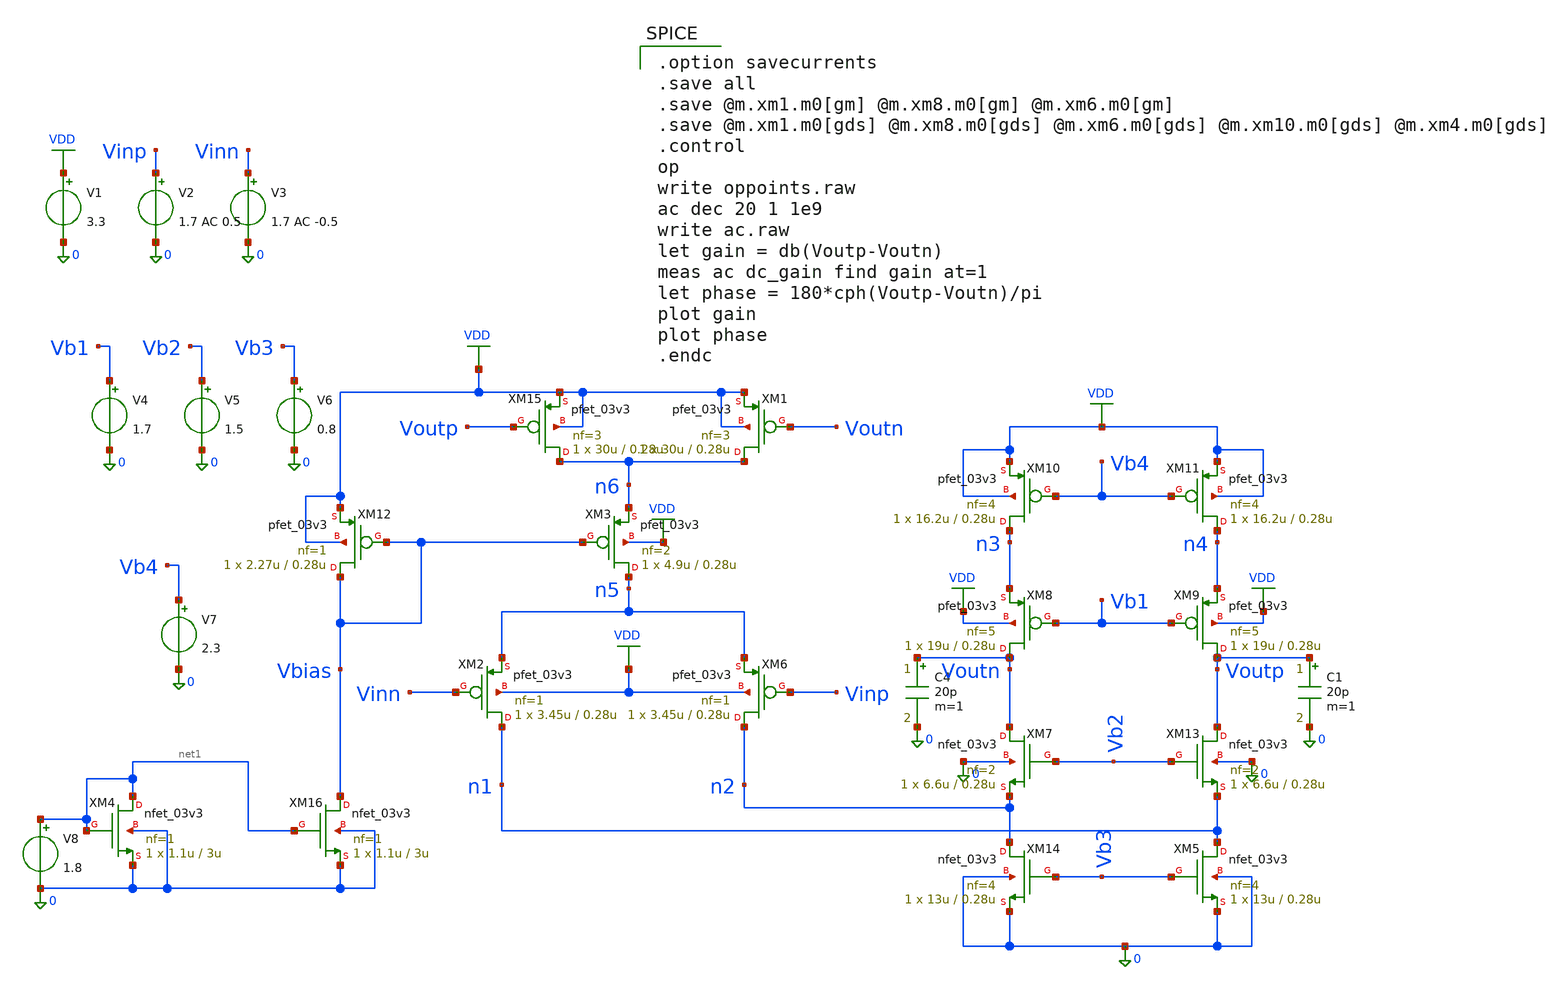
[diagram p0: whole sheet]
** sch_path: jz_fda2/xschem/foldedcasc_cmfb_forlayout_CMcheck.sch
**.subckt foldedcasc_cmfb_forlayout_CMcheck
V1 VDD 0 3.3
V2 Vinp 0 1.7 AC 0.5
C4 Voutn 0 20p m=1
C1 Voutp 0 20p m=1
V3 Vinn 0 1.7 AC -0.5
V4 Vb1 0 1.7
V5 Vb2 0 1.5
V6 Vb3 0 0.8
V7 Vb4 0 2.3
XM15 n6 Voutp VDD VDD pfet_03v3 L=0.28u W=30u nf=3 ad='int((nf+1)/2) * W/nf * 0.18u' as='int((nf+2)/2) * W/nf * 0.18u'
+ pd='2*int((nf+1)/2) * (W/nf + 0.18u)' ps='2*int((nf+2)/2) * (W/nf + 0.18u)' nrd='0.18u / W' nrs='0.18u / W'
+ sa=0 sb=0 sd=0 m=1
XM1 n6 Voutn VDD VDD pfet_03v3 L=0.28u W=30u nf=3 ad='int((nf+1)/2) * W/nf * 0.18u' as='int((nf+2)/2) * W/nf * 0.18u'
+ pd='2*int((nf+1)/2) * (W/nf + 0.18u)' ps='2*int((nf+2)/2) * (W/nf + 0.18u)' nrd='0.18u / W' nrs='0.18u / W'
+ sa=0 sb=0 sd=0 m=1
XM12 Vbias Vbias VDD VDD pfet_03v3 L=0.28u W=2.27u nf=1 ad='int((nf+1)/2) * W/nf * 0.18u' as='int((nf+2)/2) * W/nf * 0.18u'
+ pd='2*int((nf+1)/2) * (W/nf + 0.18u)' ps='2*int((nf+2)/2) * (W/nf + 0.18u)' nrd='0.18u / W' nrs='0.18u / W'
+ sa=0 sb=0 sd=0 m=1
XM3 n5 Vbias n6 VDD pfet_03v3 L=0.28u W=4.9u nf=2 ad='int((nf+1)/2) * W/nf * 0.18u' as='int((nf+2)/2) * W/nf * 0.18u'
+ pd='2*int((nf+1)/2) * (W/nf + 0.18u)' ps='2*int((nf+2)/2) * (W/nf + 0.18u)' nrd='0.18u / W' nrs='0.18u / W'
+ sa=0 sb=0 sd=0 m=1
XM2 n1 Vinn n5 VDD pfet_03v3 L=0.28u W=3.45u nf=1 ad='int((nf+1)/2) * W/nf * 0.18u' as='int((nf+2)/2) * W/nf * 0.18u'
+ pd='2*int((nf+1)/2) * (W/nf + 0.18u)' ps='2*int((nf+2)/2) * (W/nf + 0.18u)' nrd='0.18u / W' nrs='0.18u / W'
+ sa=0 sb=0 sd=0 m=1
XM6 n2 Vinp n5 VDD pfet_03v3 L=0.28u W=3.45u nf=1 ad='int((nf+1)/2) * W/nf * 0.18u' as='int((nf+2)/2) * W/nf * 0.18u'
+ pd='2*int((nf+1)/2) * (W/nf + 0.18u)' ps='2*int((nf+2)/2) * (W/nf + 0.18u)' nrd='0.18u / W' nrs='0.18u / W'
+ sa=0 sb=0 sd=0 m=1
XM10 n3 Vb4 VDD VDD pfet_03v3 L=0.28u W=16.2u nf=4 ad='int((nf+1)/2) * W/nf * 0.18u' as='int((nf+2)/2) * W/nf * 0.18u'
+ pd='2*int((nf+1)/2) * (W/nf + 0.18u)' ps='2*int((nf+2)/2) * (W/nf + 0.18u)' nrd='0.18u / W' nrs='0.18u / W'
+ sa=0 sb=0 sd=0 m=1
XM11 n4 Vb4 VDD VDD pfet_03v3 L=0.28u W=16.2u nf=4 ad='int((nf+1)/2) * W/nf * 0.18u' as='int((nf+2)/2) * W/nf * 0.18u'
+ pd='2*int((nf+1)/2) * (W/nf + 0.18u)' ps='2*int((nf+2)/2) * (W/nf + 0.18u)' nrd='0.18u / W' nrs='0.18u / W'
+ sa=0 sb=0 sd=0 m=1
XM8 Voutn Vb1 n3 VDD pfet_03v3 L=0.28u W=19u nf=5 ad='int((nf+1)/2) * W/nf * 0.18u' as='int((nf+2)/2) * W/nf * 0.18u'
+ pd='2*int((nf+1)/2) * (W/nf + 0.18u)' ps='2*int((nf+2)/2) * (W/nf + 0.18u)' nrd='0.18u / W' nrs='0.18u / W'
+ sa=0 sb=0 sd=0 m=1
XM9 Voutp Vb1 n4 VDD pfet_03v3 L=0.28u W=19u nf=5 ad='int((nf+1)/2) * W/nf * 0.18u' as='int((nf+2)/2) * W/nf * 0.18u'
+ pd='2*int((nf+1)/2) * (W/nf + 0.18u)' ps='2*int((nf+2)/2) * (W/nf + 0.18u)' nrd='0.18u / W' nrs='0.18u / W'
+ sa=0 sb=0 sd=0 m=1
XM7 Voutn Vb2 n2 0 nfet_03v3 L=0.28u W=6.6u nf=2 ad='int((nf+1)/2) * W/nf * 0.18u' as='int((nf+2)/2) * W/nf * 0.18u'
+ pd='2*int((nf+1)/2) * (W/nf + 0.18u)' ps='2*int((nf+2)/2) * (W/nf + 0.18u)' nrd='0.18u / W' nrs='0.18u / W'
+ sa=0 sb=0 sd=0 m=1
XM13 Voutp Vb2 n1 0 nfet_03v3 L=0.28u W=6.6u nf=2 ad='int((nf+1)/2) * W/nf * 0.18u' as='int((nf+2)/2) * W/nf * 0.18u'
+ pd='2*int((nf+1)/2) * (W/nf + 0.18u)' ps='2*int((nf+2)/2) * (W/nf + 0.18u)' nrd='0.18u / W' nrs='0.18u / W'
+ sa=0 sb=0 sd=0 m=1
XM14 n2 Vb3 0 0 nfet_03v3 L=0.28u W=13u nf=4 ad='int((nf+1)/2) * W/nf * 0.18u' as='int((nf+2)/2) * W/nf * 0.18u'
+ pd='2*int((nf+1)/2) * (W/nf + 0.18u)' ps='2*int((nf+2)/2) * (W/nf + 0.18u)' nrd='0.18u / W' nrs='0.18u / W'
+ sa=0 sb=0 sd=0 m=1
XM5 n1 Vb3 0 0 nfet_03v3 L=0.28u W=13u nf=4 ad='int((nf+1)/2) * W/nf * 0.18u' as='int((nf+2)/2) * W/nf * 0.18u'
+ pd='2*int((nf+1)/2) * (W/nf + 0.18u)' ps='2*int((nf+2)/2) * (W/nf + 0.18u)' nrd='0.18u / W' nrs='0.18u / W'
+ sa=0 sb=0 sd=0 m=1
V8 net1 0 1.8
XM4 net1 net1 0 0 nfet_03v3 L=3u W=1.1u nf=1 ad='int((nf+1)/2) * W/nf * 0.18u' as='int((nf+2)/2) * W/nf * 0.18u'
+ pd='2*int((nf+1)/2) * (W/nf + 0.18u)' ps='2*int((nf+2)/2) * (W/nf + 0.18u)' nrd='0.18u / W' nrs='0.18u / W'
+ sa=0 sb=0 sd=0 m=1
XM16 Vbias net1 0 0 nfet_03v3 L=3u W=1.1u nf=1 ad='int((nf+1)/2) * W/nf * 0.18u' as='int((nf+2)/2) * W/nf * 0.18u'
+ pd='2*int((nf+1)/2) * (W/nf + 0.18u)' ps='2*int((nf+2)/2) * (W/nf + 0.18u)' nrd='0.18u / W' nrs='0.18u / W'
+ sa=0 sb=0 sd=0 m=1
**** begin user architecture code

.include $::180MCU_MODELS/design.ngspice
.lib $::180MCU_MODELS/sm141064.ngspice typical
.lib $::180MCU_MODELS/smbb000149.ngspice typical


.option savecurrents
.save all
.save @m.xm1.m0[gm] @m.xm8.m0[gm] @m.xm6.m0[gm]
.save @m.xm1.m0[gds] @m.xm8.m0[gds] @m.xm6.m0[gds] @m.xm10.m0[gds] @m.xm4.m0[gds]
.control
op
write oppoints.raw
ac dec 20 1 1e9
write ac.raw
let gain = db(Voutp-Voutn)
meas ac dc_gain find gain at=1
let phase = 180*cph(Voutp-Voutn)/pi
plot gain
plot phase
.endc

**** end user architecture code
**.ends
.GLOBAL VDD
.end
